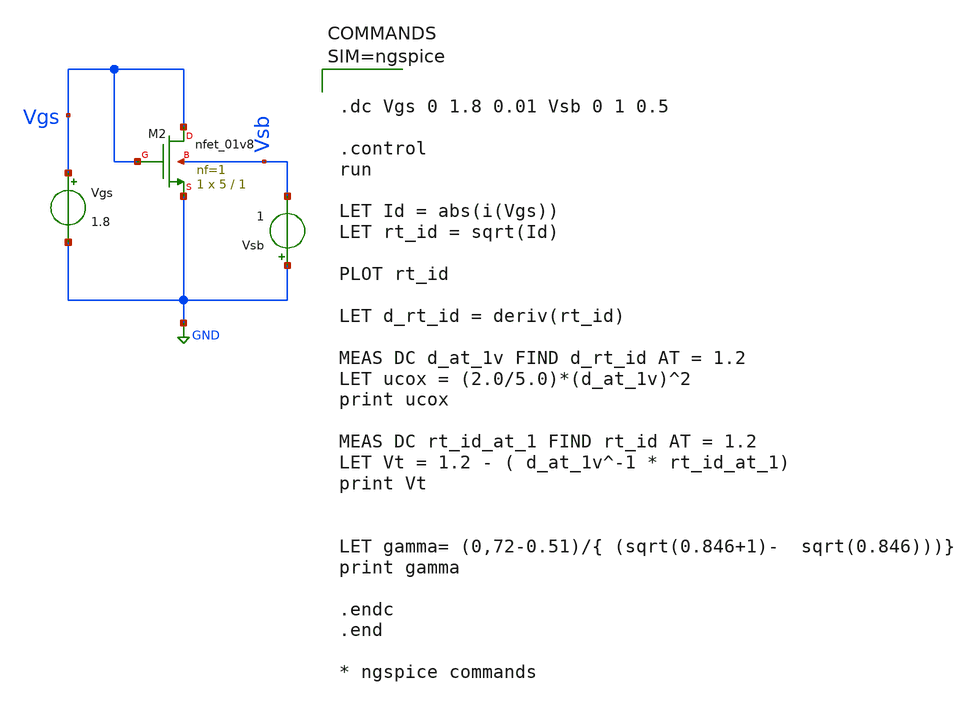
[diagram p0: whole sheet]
** sch_path: sch/lvl49-1.sch
**.subckt lvl49-1
XM2 Vgs Vgs GND Vsb sky130_fd_pr__nfet_01v8 L=1 W=5 nf=1 ad='int((1 + 1)/2) * 5 / 1 * 0.29' as='int((1 + 2)/2) * 5 / 1 * 0.29'
+ pd='2*int((1 + 1)/2) * (5 / 1 + 0.29)' ps='2*int((1 + 2)/2) * (5 / 1 + 0.29)' nrd='0.29 / 5 ' nrs='0.29 / 5 '
+ sa=0 sb=0 sd=0 mult=1 m=1
Vgs Vgs GND 1.8
Vsb GND Vsb 1
**** begin user architecture code

** opencircuitdesign pdks install
.lib $::SKYWATER_MODELS/sky130.lib.spice tt




.dc Vgs 0 1.8 0.01 Vsb 0 1 0.5

.control
run

LET Id = abs(i(Vgs))
LET rt_id = sqrt(Id)

PLOT rt_id

LET d_rt_id = deriv(rt_id)

MEAS DC d_at_1v FIND d_rt_id AT = 1.2
LET ucox = (2.0/5.0)*(d_at_1v)^2
print ucox

MEAS DC rt_id_at_1 FIND rt_id AT = 1.2
LET Vt = 1.2 - ( d_at_1v^-1 * rt_id_at_1)
print Vt


LET gamma= (0,72-0.51)/{ (sqrt(0.846+1)-  sqrt(0.846)))}
print gamma

.endc
.end

* ngspice commands



**** end user architecture code
**.ends
.GLOBAL GND
.end
